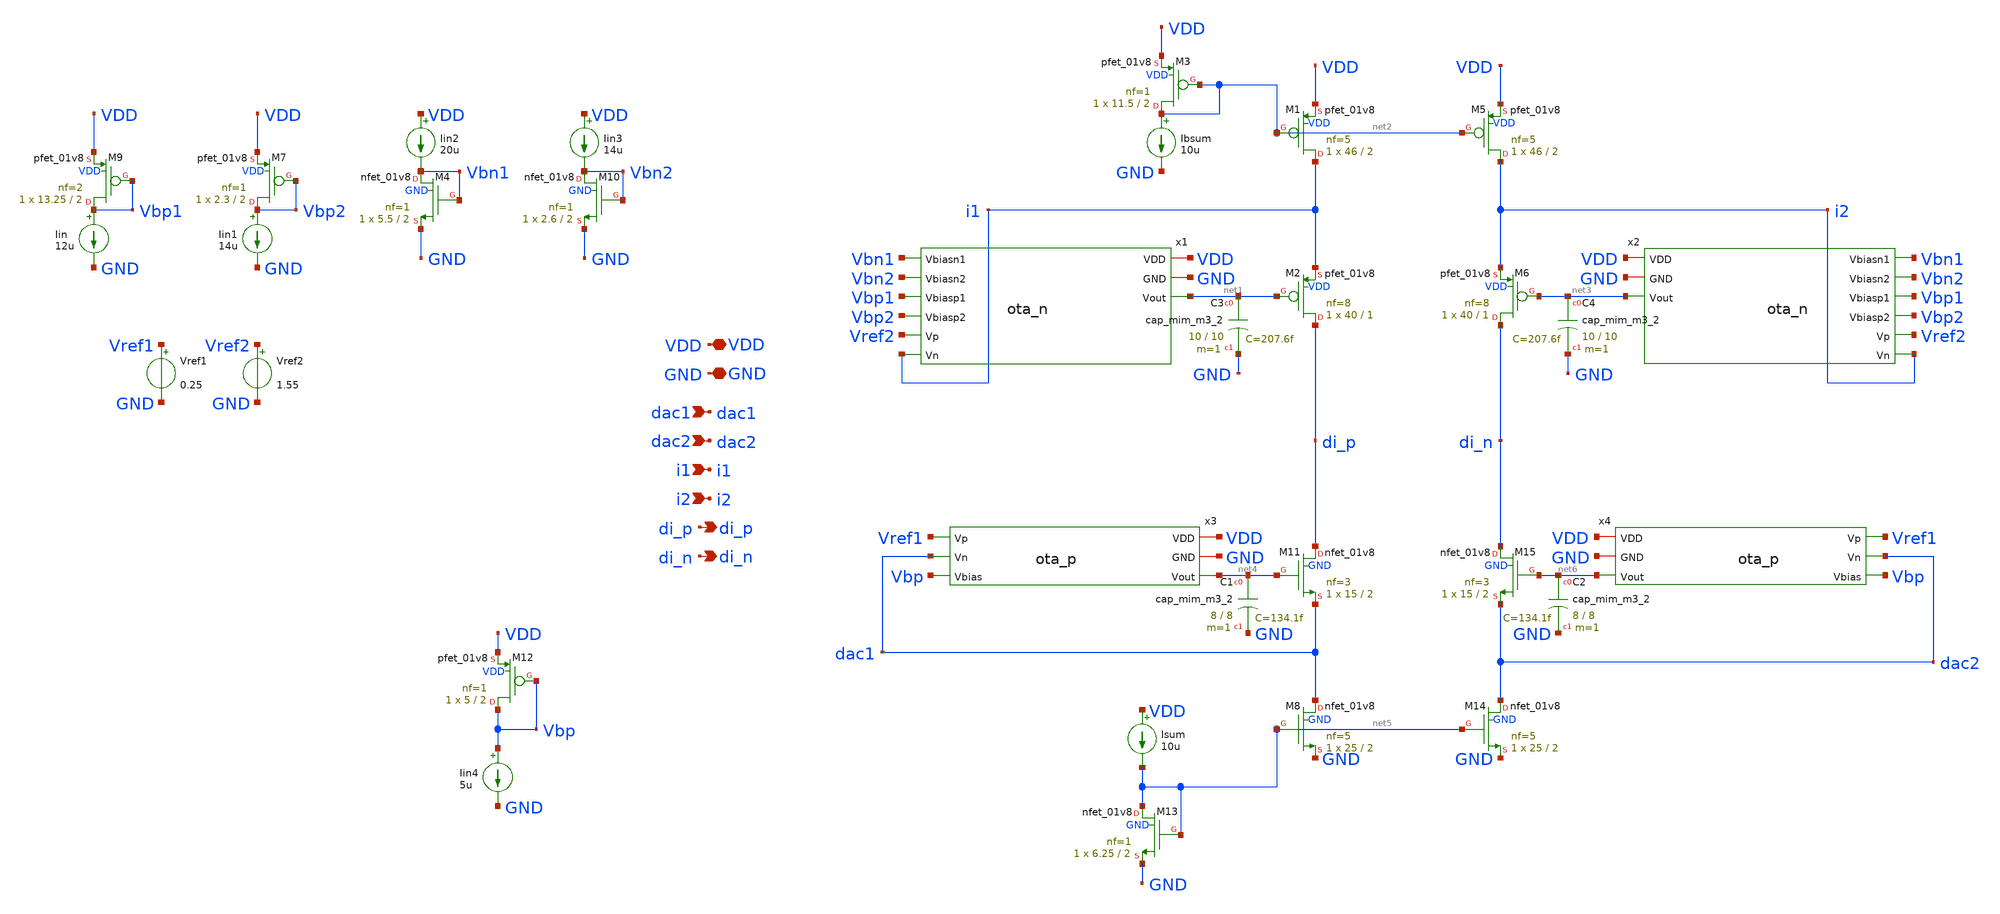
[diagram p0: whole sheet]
** sch_path: sch/summing_stage/sum_block.sch
**.subckt sum_block dac1 di_p VDD GND dac2 i1 di_n i2
*.ipin dac1
*.opin di_p
*.iopin VDD
*.iopin GND
*.ipin dac2
*.ipin i1
*.opin di_n
*.ipin i2
Vref2 Vref2 GND 1.55
.save i(vref2)
x1 VDD GND Vbn1 Vbn2 Vbp1 Vbp2 Vref2 i1 net1 ota_n
XM1 i1 net2 VDD VDD sky130_fd_pr__pfet_01v8 L=2 W=46 nf=5 ad='int((5 + 1)/2) * 46 / 5 * 0.29' as='int((5 + 2)/2) * 46 / 5 * 0.29'
+ pd='2*int((5 + 1)/2) * (46 / 5 + 0.29)' ps='2*int((5 + 2)/2) * (46 / 5 + 0.29)' nrd='0.29 / 46 ' nrs='0.29 / 46 '
+ sa=0 sb=0 sd=0 mult=1 m=1
XM2 di_p net1 i1 VDD sky130_fd_pr__pfet_01v8 L=1 W=40 nf=8 ad='int((8 + 1)/2) * 40 / 8 * 0.29' as='int((8 + 2)/2) * 40 / 8 * 0.29'
+ pd='2*int((8 + 1)/2) * (40 / 8 + 0.29)' ps='2*int((8 + 2)/2) * (40 / 8 + 0.29)' nrd='0.29 / 40 ' nrs='0.29 / 40 '
+ sa=0 sb=0 sd=0 mult=1 m=1
XM3 net2 net2 VDD VDD sky130_fd_pr__pfet_01v8 L=2 W=11.5 nf=1 ad='int((1 + 1)/2) * 11.5 / 1 * 0.29' as='int((1 + 2)/2) * 11.5 / 1 * 0.29'
+ pd='2*int((1 + 1)/2) * (11.5 / 1 + 0.29)' ps='2*int((1 + 2)/2) * (11.5 / 1 + 0.29)' nrd='0.29 / 11.5 '
+ nrs='0.29 / 11.5 ' sa=0 sb=0 sd=0 mult=1 m=1
Ibsum net2 GND 10u
Iin Vbp1 GND 12u
Iin1 Vbp2 GND 14u
Iin2 VDD Vbn1 20u
Iin3 VDD Vbn2 14u
XM9 Vbp1 Vbp1 VDD VDD sky130_fd_pr__pfet_01v8 L=2 W=13.25 nf=2 ad='int((2 + 1)/2) * 13.25 / 2 * 0.29'
+ as='int((2 + 2)/2) * 13.25 / 2 * 0.29' pd='2*int((2 + 1)/2) * (13.25 / 2 + 0.29)' ps='2*int((2 + 2)/2) * (13.25 / 2 + 0.29)'
+ nrd='0.29 / 13.25 ' nrs='0.29 / 13.25 ' sa=0 sb=0 sd=0 mult=1 m=1
XM7 Vbp2 Vbp2 VDD VDD sky130_fd_pr__pfet_01v8 L=2 W=2.3 nf=1 ad='int((1 + 1)/2) * 2.3 / 1 * 0.29' as='int((1 + 2)/2) * 2.3 / 1 * 0.29'
+ pd='2*int((1 + 1)/2) * (2.3 / 1 + 0.29)' ps='2*int((1 + 2)/2) * (2.3 / 1 + 0.29)' nrd='0.29 / 2.3 ' nrs='0.29 / 2.3 '
+ sa=0 sb=0 sd=0 mult=1 m=1
XM10 Vbn2 Vbn2 GND GND sky130_fd_pr__nfet_01v8 L=2 W=2.6 nf=1 ad='int((1 + 1)/2) * 2.6 / 1 * 0.29' as='int((1 + 2)/2) * 2.6 / 1 * 0.29'
+ pd='2*int((1 + 1)/2) * (2.6 / 1 + 0.29)' ps='2*int((1 + 2)/2) * (2.6 / 1 + 0.29)' nrd='0.29 / 2.6 ' nrs='0.29 / 2.6 '
+ sa=0 sb=0 sd=0 mult=1 m=1
XM4 Vbn1 Vbn1 GND GND sky130_fd_pr__nfet_01v8 L=2 W=5.5 nf=1 ad='int((1 + 1)/2) * 5.5 / 1 * 0.29' as='int((1 + 2)/2) * 5.5 / 1 * 0.29'
+ pd='2*int((1 + 1)/2) * (5.5 / 1 + 0.29)' ps='2*int((1 + 2)/2) * (5.5 / 1 + 0.29)' nrd='0.29 / 5.5 ' nrs='0.29 / 5.5 '
+ sa=0 sb=0 sd=0 mult=1 m=1
x2 VDD GND Vbn1 Vbn2 Vbp1 Vbp2 Vref2 i2 net3 ota_n
XM5 i2 net2 VDD VDD sky130_fd_pr__pfet_01v8 L=2 W=46 nf=5 ad='int((5 + 1)/2) * 46 / 5 * 0.29' as='int((5 + 2)/2) * 46 / 5 * 0.29'
+ pd='2*int((5 + 1)/2) * (46 / 5 + 0.29)' ps='2*int((5 + 2)/2) * (46 / 5 + 0.29)' nrd='0.29 / 46 ' nrs='0.29 / 46 '
+ sa=0 sb=0 sd=0 mult=1 m=1
XM6 di_n net3 i2 VDD sky130_fd_pr__pfet_01v8 L=1 W=40 nf=8 ad='int((8 + 1)/2) * 40 / 8 * 0.29' as='int((8 + 2)/2) * 40 / 8 * 0.29'
+ pd='2*int((8 + 1)/2) * (40 / 8 + 0.29)' ps='2*int((8 + 2)/2) * (40 / 8 + 0.29)' nrd='0.29 / 40 ' nrs='0.29 / 40 '
+ sa=0 sb=0 sd=0 mult=1 m=1
XM8 dac1 net5 GND GND sky130_fd_pr__nfet_01v8 L=2 W=25 nf=5 ad='int((5 + 1)/2) * 25 / 5 * 0.29' as='int((5 + 2)/2) * 25 / 5 * 0.29'
+ pd='2*int((5 + 1)/2) * (25 / 5 + 0.29)' ps='2*int((5 + 2)/2) * (25 / 5 + 0.29)' nrd='0.29 / 25 ' nrs='0.29 / 25 '
+ sa=0 sb=0 sd=0 mult=1 m=1
XM11 di_p net4 dac1 GND sky130_fd_pr__nfet_01v8 L=2 W=15 nf=3 ad='int((3 + 1)/2) * 15 / 3 * 0.29' as='int((3 + 2)/2) * 15 / 3 * 0.29'
+ pd='2*int((3 + 1)/2) * (15 / 3 + 0.29)' ps='2*int((3 + 2)/2) * (15 / 3 + 0.29)' nrd='0.29 / 15 ' nrs='0.29 / 15 '
+ sa=0 sb=0 sd=0 mult=1 m=1
x3 VDD GND Vbp Vref1 dac1 net4 ota_p
Vref1 Vref1 GND 0.25
.save i(vref1)
Iin4 Vbp GND 5u
XM12 Vbp Vbp VDD VDD sky130_fd_pr__pfet_01v8 L=2 W=5 nf=1 ad='int((1 + 1)/2) * 5 / 1 * 0.29' as='int((1 + 2)/2) * 5 / 1 * 0.29'
+ pd='2*int((1 + 1)/2) * (5 / 1 + 0.29)' ps='2*int((1 + 2)/2) * (5 / 1 + 0.29)' nrd='0.29 / 5 ' nrs='0.29 / 5 '
+ sa=0 sb=0 sd=0 mult=1 m=1
Isum VDD net5 10u
XC1 net4 GND sky130_fd_pr__cap_mim_m3_2 W=8 L=8 MF=1 m=1
XM13 net5 net5 GND GND sky130_fd_pr__nfet_01v8 L=2 W=6.25 nf=1 ad='int((1 + 1)/2) * 6.25 / 1 * 0.29'
+ as='int((1 + 2)/2) * 6.25 / 1 * 0.29' pd='2*int((1 + 1)/2) * (6.25 / 1 + 0.29)' ps='2*int((1 + 2)/2) * (6.25 / 1 + 0.29)'
+ nrd='0.29 / 6.25 ' nrs='0.29 / 6.25 ' sa=0 sb=0 sd=0 mult=1 m=1
XM14 dac2 net5 GND GND sky130_fd_pr__nfet_01v8 L=2 W=25 nf=5 ad='int((5 + 1)/2) * 25 / 5 * 0.29' as='int((5 + 2)/2) * 25 / 5 * 0.29'
+ pd='2*int((5 + 1)/2) * (25 / 5 + 0.29)' ps='2*int((5 + 2)/2) * (25 / 5 + 0.29)' nrd='0.29 / 25 ' nrs='0.29 / 25 '
+ sa=0 sb=0 sd=0 mult=1 m=1
XM15 di_n net6 dac2 GND sky130_fd_pr__nfet_01v8 L=2 W=15 nf=3 ad='int((3 + 1)/2) * 15 / 3 * 0.29' as='int((3 + 2)/2) * 15 / 3 * 0.29'
+ pd='2*int((3 + 1)/2) * (15 / 3 + 0.29)' ps='2*int((3 + 2)/2) * (15 / 3 + 0.29)' nrd='0.29 / 15 ' nrs='0.29 / 15 '
+ sa=0 sb=0 sd=0 mult=1 m=1
x4 VDD GND Vbp Vref1 dac2 net6 ota_p
XC2 net6 GND sky130_fd_pr__cap_mim_m3_2 W=8 L=8 MF=1 m=1
XC3 net1 GND sky130_fd_pr__cap_mim_m3_2 W=10 L=10 MF=1 m=1
XC4 net3 GND sky130_fd_pr__cap_mim_m3_2 W=10 L=10 MF=1 m=1
**.ends

* expanding   symbol:  cascode/ota_n.sym # of pins=9
** sym_path: sch/cascode/ota_n.sym
** sch_path: sch/cascode/ota_n.sch
.subckt ota_n VDD GND Vbiasn1 Vbiasn2 Vbiasp1 Vbiasp2 Vp Vn Vout
*.ipin Vbiasn2
*.opin Vout
*.iopin VDD
*.iopin GND
*.ipin Vp
*.ipin Vn
*.ipin Vbiasp1
*.ipin Vbiasp2
*.ipin Vbiasn1
XM3 net1 Vp Vx GND sky130_fd_pr__nfet_01v8 L=2 W=7.5 nf=1 ad='int((1 + 1)/2) * 7.5 / 1 * 0.29' as='int((1 + 2)/2) * 7.5 / 1 * 0.29'
+ pd='2*int((1 + 1)/2) * (7.5 / 1 + 0.29)' ps='2*int((1 + 2)/2) * (7.5 / 1 + 0.29)' nrd='0.29 / 7.5 ' nrs='0.29 / 7.5 '
+ sa=0 sb=0 sd=0 mult=1 m=1
XM2 Vfold Vn Vx GND sky130_fd_pr__nfet_01v8 L=2 W=7.5 nf=1 ad='int((1 + 1)/2) * 7.5 / 1 * 0.29' as='int((1 + 2)/2) * 7.5 / 1 * 0.29'
+ pd='2*int((1 + 1)/2) * (7.5 / 1 + 0.29)' ps='2*int((1 + 2)/2) * (7.5 / 1 + 0.29)' nrd='0.29 / 7.5 ' nrs='0.29 / 7.5 '
+ sa=0 sb=0 sd=0 mult=1 m=1
XM4 net3 net2 GND GND sky130_fd_pr__nfet_01v8 L=2 W=14 nf=2 ad='int((2 + 1)/2) * 14 / 2 * 0.29' as='int((2 + 2)/2) * 14 / 2 * 0.29'
+ pd='2*int((2 + 1)/2) * (14 / 2 + 0.29)' ps='2*int((2 + 2)/2) * (14 / 2 + 0.29)' nrd='0.29 / 14 ' nrs='0.29 / 14 '
+ sa=0 sb=0 sd=0 mult=1 m=1
XM5 net4 net2 GND GND sky130_fd_pr__nfet_01v8 L=2 W=14 nf=2 ad='int((2 + 1)/2) * 14 / 2 * 0.29' as='int((2 + 2)/2) * 14 / 2 * 0.29'
+ pd='2*int((2 + 1)/2) * (14 / 2 + 0.29)' ps='2*int((2 + 2)/2) * (14 / 2 + 0.29)' nrd='0.29 / 14 ' nrs='0.29 / 14 '
+ sa=0 sb=0 sd=0 mult=1 m=1
XM8 net1 Vbiasp1 VDD VDD sky130_fd_pr__pfet_01v8 L=2 W=26.5 nf=5 ad='int((5 + 1)/2) * 26.5 / 5 * 0.29'
+ as='int((5 + 2)/2) * 26.5 / 5 * 0.29' pd='2*int((5 + 1)/2) * (26.5 / 5 + 0.29)' ps='2*int((5 + 2)/2) * (26.5 / 5 + 0.29)'
+ nrd='0.29 / 26.5 ' nrs='0.29 / 26.5 ' sa=0 sb=0 sd=0 mult=1 m=1
XM9 Vfold Vbiasp1 VDD VDD sky130_fd_pr__pfet_01v8 L=2 W=26.5 nf=5 ad='int((5 + 1)/2) * 26.5 / 5 * 0.29'
+ as='int((5 + 2)/2) * 26.5 / 5 * 0.29' pd='2*int((5 + 1)/2) * (26.5 / 5 + 0.29)' ps='2*int((5 + 2)/2) * (26.5 / 5 + 0.29)'
+ nrd='0.29 / 26.5 ' nrs='0.29 / 26.5 ' sa=0 sb=0 sd=0 mult=1 m=1
XM1 Vx Vbiasn1 GND GND sky130_fd_pr__nfet_01v8 L=2 W=5.5 nf=1 ad='int((1 + 1)/2) * 5.5 / 1 * 0.29' as='int((1 + 2)/2) * 5.5 / 1 * 0.29'
+ pd='2*int((1 + 1)/2) * (5.5 / 1 + 0.29)' ps='2*int((1 + 2)/2) * (5.5 / 1 + 0.29)' nrd='0.29 / 5.5 ' nrs='0.29 / 5.5 '
+ sa=0 sb=0 sd=0 mult=1 m=1
XM6 net2 Vbiasp2 net1 VDD sky130_fd_pr__pfet_01v8 L=2 W=13 nf=2 ad='int((2 + 1)/2) * 13 / 2 * 0.29' as='int((2 + 2)/2) * 13 / 2 * 0.29'
+ pd='2*int((2 + 1)/2) * (13 / 2 + 0.29)' ps='2*int((2 + 2)/2) * (13 / 2 + 0.29)' nrd='0.29 / 13 ' nrs='0.29 / 13 '
+ sa=0 sb=0 sd=0 mult=1 m=1
XM7 Vout Vbiasp2 Vfold VDD sky130_fd_pr__pfet_01v8 L=2 W=13 nf=2 ad='int((2 + 1)/2) * 13 / 2 * 0.29'
+ as='int((2 + 2)/2) * 13 / 2 * 0.29' pd='2*int((2 + 1)/2) * (13 / 2 + 0.29)' ps='2*int((2 + 2)/2) * (13 / 2 + 0.29)'
+ nrd='0.29 / 13 ' nrs='0.29 / 13 ' sa=0 sb=0 sd=0 mult=1 m=1
XM10 Vout Vbiasn2 net4 GND sky130_fd_pr__nfet_01v8 L=2 W=26.5 nf=5 ad='int((5 + 1)/2) * 26.5 / 5 * 0.29'
+ as='int((5 + 2)/2) * 26.5 / 5 * 0.29' pd='2*int((5 + 1)/2) * (26.5 / 5 + 0.29)' ps='2*int((5 + 2)/2) * (26.5 / 5 + 0.29)'
+ nrd='0.29 / 26.5 ' nrs='0.29 / 26.5 ' sa=0 sb=0 sd=0 mult=1 m=1
XM11 net2 Vbiasn2 net3 GND sky130_fd_pr__nfet_01v8 L=2 W=26.5 nf=5 ad='int((5 + 1)/2) * 26.5 / 5 * 0.29'
+ as='int((5 + 2)/2) * 26.5 / 5 * 0.29' pd='2*int((5 + 1)/2) * (26.5 / 5 + 0.29)' ps='2*int((5 + 2)/2) * (26.5 / 5 + 0.29)'
+ nrd='0.29 / 26.5 ' nrs='0.29 / 26.5 ' sa=0 sb=0 sd=0 mult=1 m=1
.ends


* expanding   symbol:  cascode/ota_p.sym # of pins=6
** sym_path: sch/cascode/ota_p.sym
** sch_path: sch/cascode/ota_p.sch
.subckt ota_p VDD GND Vbias Vp Vn Vout
*.ipin Vbias
*.opin Vout
*.iopin VDD
*.iopin GND
*.ipin Vp
*.ipin Vn
XM1 net1 Vp Vx VDD sky130_fd_pr__pfet_01v8 L=2 W=25 nf=5 ad='int((5 + 1)/2) * 25 / 5 * 0.29' as='int((5 + 2)/2) * 25 / 5 * 0.29'
+ pd='2*int((5 + 1)/2) * (25 / 5 + 0.29)' ps='2*int((5 + 2)/2) * (25 / 5 + 0.29)' nrd='0.29 / 25 ' nrs='0.29 / 25 '
+ sa=0 sb=0 sd=0 mult=1 m=1
XM2 Vout Vn Vx VDD sky130_fd_pr__pfet_01v8 L=2 W=25 nf=5 ad='int((5 + 1)/2) * 25 / 5 * 0.29' as='int((5 + 2)/2) * 25 / 5 * 0.29'
+ pd='2*int((5 + 1)/2) * (25 / 5 + 0.29)' ps='2*int((5 + 2)/2) * (25 / 5 + 0.29)' nrd='0.29 / 25 ' nrs='0.29 / 25 '
+ sa=0 sb=0 sd=0 mult=1 m=1
XM3 net1 net1 GND GND sky130_fd_pr__nfet_01v8 L=2 W=1.5 nf=1 ad='int((1 + 1)/2) * 1.5 / 1 * 0.29' as='int((1 + 2)/2) * 1.5 / 1 * 0.29'
+ pd='2*int((1 + 1)/2) * (1.5 / 1 + 0.29)' ps='2*int((1 + 2)/2) * (1.5 / 1 + 0.29)' nrd='0.29 / 1.5 ' nrs='0.29 / 1.5 '
+ sa=0 sb=0 sd=0 mult=1 m=1
XM4 Vout net1 GND GND sky130_fd_pr__nfet_01v8 L=2 W=1.5 nf=1 ad='int((1 + 1)/2) * 1.5 / 1 * 0.29' as='int((1 + 2)/2) * 1.5 / 1 * 0.29'
+ pd='2*int((1 + 1)/2) * (1.5 / 1 + 0.29)' ps='2*int((1 + 2)/2) * (1.5 / 1 + 0.29)' nrd='0.29 / 1.5 ' nrs='0.29 / 1.5 '
+ sa=0 sb=0 sd=0 mult=1 m=1
XM5 Vx Vbias VDD VDD sky130_fd_pr__pfet_01v8 L=2 W=10 nf=2 ad='int((2 + 1)/2) * 10 / 2 * 0.29' as='int((2 + 2)/2) * 10 / 2 * 0.29'
+ pd='2*int((2 + 1)/2) * (10 / 2 + 0.29)' ps='2*int((2 + 2)/2) * (10 / 2 + 0.29)' nrd='0.29 / 10 ' nrs='0.29 / 10 '
+ sa=0 sb=0 sd=0 mult=1 m=1
.ends

.end
